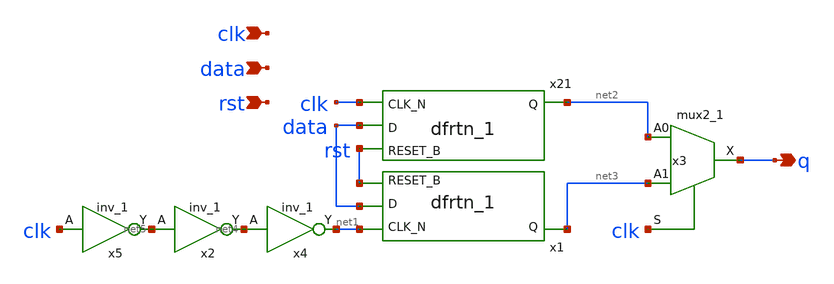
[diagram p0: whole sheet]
** sch_path: xschem/tryandtest/deff_rst.sch
**.subckt deff_rst clk data q rst
*.ipin clk
*.ipin data
*.opin q
*.ipin rst
x3 net2 net3 clk GND GND VDD VDD q sky130_fd_sc_lp__mux2_1
x4 net4 GND GND VDD VDD net1 sky130_fd_sc_lp__inv_1
x21 clk data rst GND GND VDD VDD net2 sky130_fd_sc_lp__dfrtn_1
x1 net1 data rst GND GND VDD VDD net3 sky130_fd_sc_lp__dfrtn_1
x2 net5 GND GND VDD VDD net4 sky130_fd_sc_lp__inv_1
x5 clk GND GND VDD VDD net5 sky130_fd_sc_lp__inv_1
**.ends
.end
